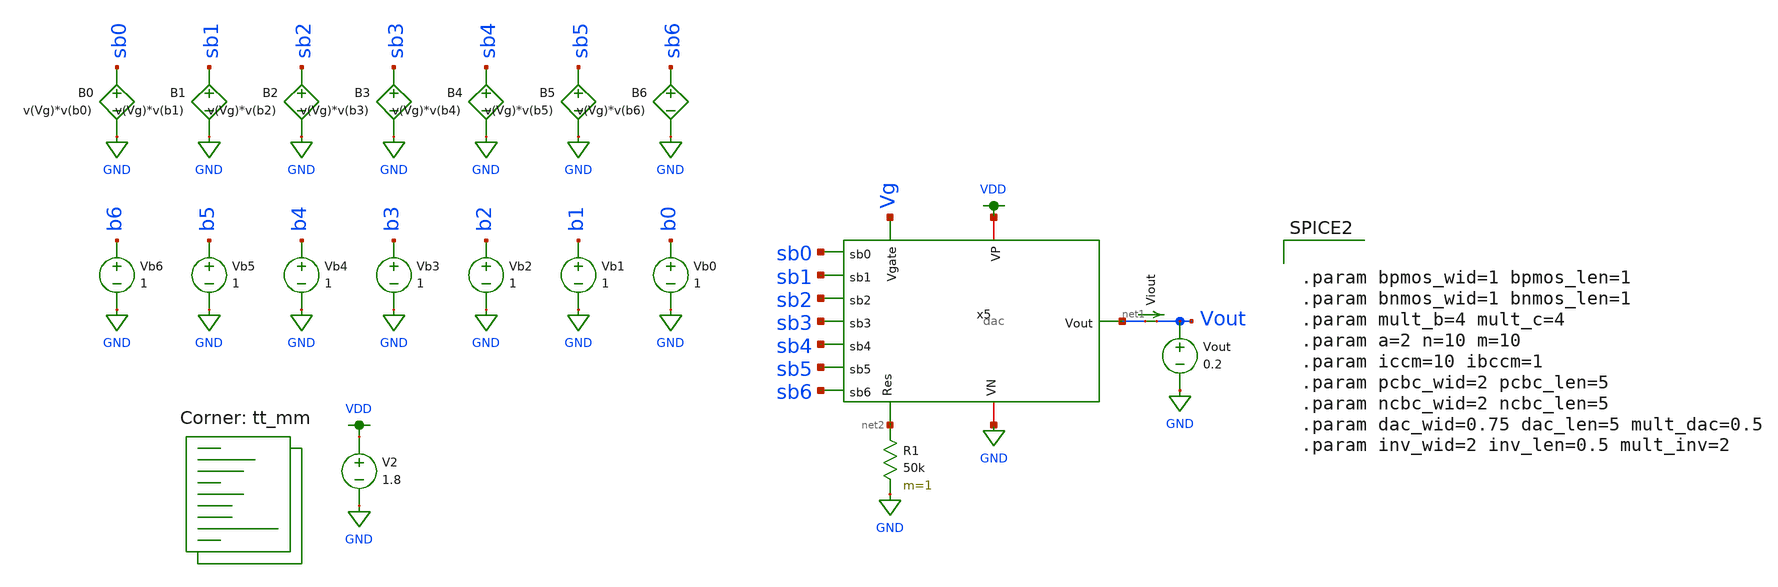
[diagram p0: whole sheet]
** sch_path: test_dac.sch
**.subckt test_dac
V2 VDD GND 1.8
R1 net2 GND 50k m=1
Vout Vout GND 0.2
Viout net1 Vout 0
.save i(viout)
Vb0 b0 GND 1
B0 sb0 GND V=v(Vg)*v(b0)
Vb1 b1 GND 1
B1 sb1 GND V=v(Vg)*v(b1)
Vb2 b2 GND 1
B2 sb2 GND V=v(Vg)*v(b2)
Vb3 b3 GND 1
B3 sb3 GND V=v(Vg)*v(b3)
Vb4 b4 GND 1
B4 sb4 GND V=v(Vg)*v(b4)
Vb5 b5 GND 1
B5 sb5 GND V=v(Vg)*v(b5)
Vb6 b6 GND 1
B6 sb6 GND V=v(Vg)*v(b6)
x5 VDD sb0 sb1 GND sb2 net1 Vg sb3 sb4 sb5 sb6 net2 dac
**** begin user architecture code
.lib $::SKYWATER_MODELS/sky130.lib.spice tt_mm


.control
  let mc_runs = 10
  let run = 1
  dowhile run <= mc_runs
    set wr_vecnames
    set appendwrite = FALSE
    set wr_singlescale
    let code = 0
    while code < 128
      if code eq 0
        let b0 = 0
      else
        let b0 = code % 2
      end
      if floor(code / 2) eq 0
        let b1 = 0
      else
        let b1 = floor(code / 2) % 2
      end
      if floor(code / 4) eq 0
        let b2 = 0
      else
        let b2 = floor(code / 4) % 2
      end
      if floor(code / 8) eq 0
        let b3 = 0
      else
        let b3 = floor(code / 8) % 2
      end
      if floor(code / 16) eq 0
        let b4 = 0
      else
        let b4 = floor(code / 16) % 2
      end
      if floor(code / 32) eq 0
        let b5 = 0
      else
        let b5 = floor(code / 32) % 2
      end
      if floor(code / 64) eq 0
        let b6 = 0
      else
        let b6 = floor(code / 64) % 2
      end
      alter vb0 $&b0
      alter vb1 $&b1
      alter vb2 $&b2
      alter vb3 $&b3
      alter vb4 $&b4
      alter vb5 $&b5
      alter vb6 $&b6
      save all
      op
      wrdata ~/Documents/mosfet-dac/test_dac{$&run}.txt code v(sb0) v(sb1) v(sb2) v(sb3) v(sb4) v(sb5)
+ v(sb6) i(Viout) v(Vout)
      if code eq 0
        set appendwrite
        set wr_vecnames = FALSE
      end
      let code = code + 1
    end
    reset
    let run = run + 1
  end
quit
.endc



.param bpmos_wid=1 bpmos_len=1
.param bnmos_wid=1 bnmos_len=1
.param mult_b=4 mult_c=4
.param a=2 n=10 m=10
.param iccm=10 ibccm=1
.param pcbc_wid=2 pcbc_len=5
.param ncbc_wid=2 ncbc_len=5
.param dac_wid=0.75 dac_len=5 mult_dac=0.5
.param inv_wid=2 inv_len=0.5 mult_inv=2


**** end user architecture code
**.ends
.GLOBAL GND
.GLOBAL VDD
.end
